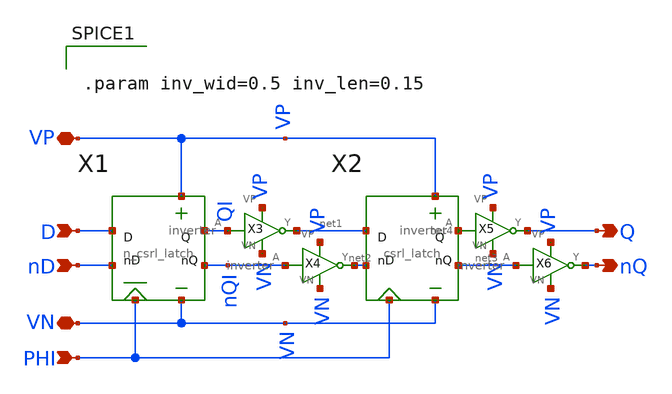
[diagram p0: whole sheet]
** sch_path: dff.sch
**.subckt dff VP D Q nD PHI nQ VN
*.iopin VP
*.ipin D
*.opin Q
*.ipin nD
*.ipin PHI
*.opin nQ
*.iopin VN
X1 VN VP nQI QI PHI nD D n_csrl_latch
X2 VN VP net3 net4 PHI net2 net1 csrl_latch
X3 QI net1 VP VN inverter
X4 nQI net2 VP VN inverter
X5 net4 Q VP VN inverter
X6 net3 nQ VP VN inverter
**** begin user architecture code


.param inv_wid=0.5 inv_len=0.15


**** end user architecture code
**.ends

* expanding   symbol:  n_csrl_latch.sym # of pins=7
** sym_path: n_csrl_latch.sym
** sch_path: n_csrl_latch.sch
.subckt n_csrl_latch VN VP nQ Q PHI nD D
*.ipin D
*.ipin nD
*.opin nQ
*.opin Q
*.ipin PHI
*.iopin VP
*.iopin VN
XM1 VN nD net3 VN sky130_fd_pr__nfet_01v8 L={dff_len} W={dff_wid} nf=1 ad='int((nf+1)/2) * W/nf * 0.29'
+ as='int((nf+2)/2) * W/nf * 0.29' pd='2*int((nf+1)/2) * (W/nf + 0.29)' ps='2*int((nf+2)/2) * (W/nf + 0.29)'
+ nrd='0.29 / W' nrs='0.29 / W' sa=0 sb=0 sd=0 mult=1 m=1
XM2 net3 PHI Q VN sky130_fd_pr__nfet_01v8 L={dff_len} W={dff_wid} nf=1 ad='int((nf+1)/2) * W/nf * 0.29'
+ as='int((nf+2)/2) * W/nf * 0.29' pd='2*int((nf+1)/2) * (W/nf + 0.29)' ps='2*int((nf+2)/2) * (W/nf + 0.29)'
+ nrd='0.29 / W' nrs='0.29 / W' sa=0 sb=0 sd=0 mult=1 m=1
XM3 VN nQ Q VN sky130_fd_pr__nfet_01v8 L={dff_len} W={dff_wid} nf=1 ad='int((nf+1)/2) * W/nf * 0.29'
+ as='int((nf+2)/2) * W/nf * 0.29' pd='2*int((nf+1)/2) * (W/nf + 0.29)' ps='2*int((nf+2)/2) * (W/nf + 0.29)'
+ nrd='0.29 / W' nrs='0.29 / W' sa=0 sb=0 sd=0 mult=1 m=1
XM4 net1 D VN VN sky130_fd_pr__nfet_01v8 L={dff_len} W={dff_wid} nf=1 ad='int((nf+1)/2) * W/nf * 0.29'
+ as='int((nf+2)/2) * W/nf * 0.29' pd='2*int((nf+1)/2) * (W/nf + 0.29)' ps='2*int((nf+2)/2) * (W/nf + 0.29)'
+ nrd='0.29 / W' nrs='0.29 / W' sa=0 sb=0 sd=0 mult=1 m=1
XM5 net1 PHI nQ VN sky130_fd_pr__nfet_01v8 L={dff_len} W={dff_wid} nf=1 ad='int((nf+1)/2) * W/nf * 0.29'
+ as='int((nf+2)/2) * W/nf * 0.29' pd='2*int((nf+1)/2) * (W/nf + 0.29)' ps='2*int((nf+2)/2) * (W/nf + 0.29)'
+ nrd='0.29 / W' nrs='0.29 / W' sa=0 sb=0 sd=0 mult=1 m=1
XM6 VN Q nQ VN sky130_fd_pr__nfet_01v8 L={dff_len} W={dff_wid} nf=1 ad='int((nf+1)/2) * W/nf * 0.29'
+ as='int((nf+2)/2) * W/nf * 0.29' pd='2*int((nf+1)/2) * (W/nf + 0.29)' ps='2*int((nf+2)/2) * (W/nf + 0.29)'
+ nrd='0.29 / W' nrs='0.29 / W' sa=0 sb=0 sd=0 mult=1 m=1
XM13 VP D net2 VP sky130_fd_pr__pfet_01v8 L={dff_len} W={dff_wid} nf=1 ad='int((nf+1)/2) * W/nf * 0.29'
+ as='int((nf+2)/2) * W/nf * 0.29' pd='2*int((nf+1)/2) * (W/nf + 0.29)' ps='2*int((nf+2)/2) * (W/nf + 0.29)'
+ nrd='0.29 / W' nrs='0.29 / W' sa=0 sb=0 sd=0 mult=1 m=1
XM14 net2 PHI VP VP sky130_fd_pr__pfet_01v8 L={dff_len} W={dff_wid} nf=1 ad='int((nf+1)/2) * W/nf * 0.29'
+ as='int((nf+2)/2) * W/nf * 0.29' pd='2*int((nf+1)/2) * (W/nf + 0.29)' ps='2*int((nf+2)/2) * (W/nf + 0.29)'
+ nrd='0.29 / W' nrs='0.29 / W' sa=0 sb=0 sd=0 mult=1 m=1
XM15 nQ Q net2 VP sky130_fd_pr__pfet_01v8 L={dff_len} W={dff_wid} nf=1 ad='int((nf+1)/2) * W/nf * 0.29'
+ as='int((nf+2)/2) * W/nf * 0.29' pd='2*int((nf+1)/2) * (W/nf + 0.29)' ps='2*int((nf+2)/2) * (W/nf + 0.29)'
+ nrd='0.29 / W' nrs='0.29 / W' sa=0 sb=0 sd=0 mult=1 m=1
XM16 net4 nD VP VP sky130_fd_pr__pfet_01v8 L={dff_len} W={dff_wid} nf=1 ad='int((nf+1)/2) * W/nf * 0.29'
+ as='int((nf+2)/2) * W/nf * 0.29' pd='2*int((nf+1)/2) * (W/nf + 0.29)' ps='2*int((nf+2)/2) * (W/nf + 0.29)'
+ nrd='0.29 / W' nrs='0.29 / W' sa=0 sb=0 sd=0 mult=1 m=1
XM17 net4 PHI VP VP sky130_fd_pr__pfet_01v8 L={dff_len} W={dff_wid} nf=1 ad='int((nf+1)/2) * W/nf * 0.29'
+ as='int((nf+2)/2) * W/nf * 0.29' pd='2*int((nf+1)/2) * (W/nf + 0.29)' ps='2*int((nf+2)/2) * (W/nf + 0.29)'
+ nrd='0.29 / W' nrs='0.29 / W' sa=0 sb=0 sd=0 mult=1 m=1
XM18 Q nQ net4 VP sky130_fd_pr__pfet_01v8 L={dff_len} W={dff_wid} nf=1 ad='int((nf+1)/2) * W/nf * 0.29'
+ as='int((nf+2)/2) * W/nf * 0.29' pd='2*int((nf+1)/2) * (W/nf + 0.29)' ps='2*int((nf+2)/2) * (W/nf + 0.29)'
+ nrd='0.29 / W' nrs='0.29 / W' sa=0 sb=0 sd=0 mult=1 m=1
**** begin user architecture code


.param dff_wid=0.5 dff_len=0.5


**** end user architecture code
.ends


* expanding   symbol:  csrl_latch.sym # of pins=7
** sym_path: csrl_latch.sym
** sch_path: csrl_latch.sch
.subckt csrl_latch VN VP nQ Q PHI nD D
*.ipin nD
*.ipin D
*.opin Q
*.opin nQ
*.ipin PHI
*.iopin VP
*.iopin VN
XM7 net3 D VN VN sky130_fd_pr__nfet_01v8 L={dff_len} W={dff_wid} nf=1 ad='int((nf+1)/2) * W/nf * 0.29'
+ as='int((nf+2)/2) * W/nf * 0.29' pd='2*int((nf+1)/2) * (W/nf + 0.29)' ps='2*int((nf+2)/2) * (W/nf + 0.29)'
+ nrd='0.29 / W' nrs='0.29 / W' sa=0 sb=0 sd=0 mult=1 m=1
XM8 VN PHI net3 VN sky130_fd_pr__nfet_01v8 L={dff_len} W={dff_wid} nf=1 ad='int((nf+1)/2) * W/nf * 0.29'
+ as='int((nf+2)/2) * W/nf * 0.29' pd='2*int((nf+1)/2) * (W/nf + 0.29)' ps='2*int((nf+2)/2) * (W/nf + 0.29)'
+ nrd='0.29 / W' nrs='0.29 / W' sa=0 sb=0 sd=0 mult=1 m=1
XM9 nQ Q net3 VN sky130_fd_pr__nfet_01v8 L={dff_len} W={dff_wid} nf=1 ad='int((nf+1)/2) * W/nf * 0.29'
+ as='int((nf+2)/2) * W/nf * 0.29' pd='2*int((nf+1)/2) * (W/nf + 0.29)' ps='2*int((nf+2)/2) * (W/nf + 0.29)'
+ nrd='0.29 / W' nrs='0.29 / W' sa=0 sb=0 sd=0 mult=1 m=1
XM10 VN nD net2 VN sky130_fd_pr__nfet_01v8 L={dff_len} W={dff_wid} nf=1 ad='int((nf+1)/2) * W/nf * 0.29'
+ as='int((nf+2)/2) * W/nf * 0.29' pd='2*int((nf+1)/2) * (W/nf + 0.29)' ps='2*int((nf+2)/2) * (W/nf + 0.29)'
+ nrd='0.29 / W' nrs='0.29 / W' sa=0 sb=0 sd=0 mult=1 m=1
XM11 VN PHI net2 VN sky130_fd_pr__nfet_01v8 L={dff_len} W={dff_wid} nf=1 ad='int((nf+1)/2) * W/nf * 0.29'
+ as='int((nf+2)/2) * W/nf * 0.29' pd='2*int((nf+1)/2) * (W/nf + 0.29)' ps='2*int((nf+2)/2) * (W/nf + 0.29)'
+ nrd='0.29 / W' nrs='0.29 / W' sa=0 sb=0 sd=0 mult=1 m=1
XM12 Q nQ net2 VN sky130_fd_pr__nfet_01v8 L={dff_len} W={dff_wid} nf=1 ad='int((nf+1)/2) * W/nf * 0.29'
+ as='int((nf+2)/2) * W/nf * 0.29' pd='2*int((nf+1)/2) * (W/nf + 0.29)' ps='2*int((nf+2)/2) * (W/nf + 0.29)'
+ nrd='0.29 / W' nrs='0.29 / W' sa=0 sb=0 sd=0 mult=1 m=1
XM19 net1 nD VP VP sky130_fd_pr__pfet_01v8 L={dff_len} W={dff_wid} nf=1 ad='int((nf+1)/2) * W/nf * 0.29'
+ as='int((nf+2)/2) * W/nf * 0.29' pd='2*int((nf+1)/2) * (W/nf + 0.29)' ps='2*int((nf+2)/2) * (W/nf + 0.29)'
+ nrd='0.29 / W' nrs='0.29 / W' sa=0 sb=0 sd=0 mult=1 m=1
XM20 Q PHI net1 VP sky130_fd_pr__pfet_01v8 L={dff_len} W={dff_wid} nf=1 ad='int((nf+1)/2) * W/nf * 0.29'
+ as='int((nf+2)/2) * W/nf * 0.29' pd='2*int((nf+1)/2) * (W/nf + 0.29)' ps='2*int((nf+2)/2) * (W/nf + 0.29)'
+ nrd='0.29 / W' nrs='0.29 / W' sa=0 sb=0 sd=0 mult=1 m=1
XM21 VP nQ Q VP sky130_fd_pr__pfet_01v8 L={dff_len} W={dff_wid} nf=1 ad='int((nf+1)/2) * W/nf * 0.29'
+ as='int((nf+2)/2) * W/nf * 0.29' pd='2*int((nf+1)/2) * (W/nf + 0.29)' ps='2*int((nf+2)/2) * (W/nf + 0.29)'
+ nrd='0.29 / W' nrs='0.29 / W' sa=0 sb=0 sd=0 mult=1 m=1
XM22 VP D net4 VP sky130_fd_pr__pfet_01v8 L={dff_len} W={dff_wid} nf=1 ad='int((nf+1)/2) * W/nf * 0.29'
+ as='int((nf+2)/2) * W/nf * 0.29' pd='2*int((nf+1)/2) * (W/nf + 0.29)' ps='2*int((nf+2)/2) * (W/nf + 0.29)'
+ nrd='0.29 / W' nrs='0.29 / W' sa=0 sb=0 sd=0 mult=1 m=1
XM23 nQ PHI net4 VP sky130_fd_pr__pfet_01v8 L={dff_len} W={dff_wid} nf=1 ad='int((nf+1)/2) * W/nf * 0.29'
+ as='int((nf+2)/2) * W/nf * 0.29' pd='2*int((nf+1)/2) * (W/nf + 0.29)' ps='2*int((nf+2)/2) * (W/nf + 0.29)'
+ nrd='0.29 / W' nrs='0.29 / W' sa=0 sb=0 sd=0 mult=1 m=1
XM24 VP Q nQ VP sky130_fd_pr__pfet_01v8 L={dff_len} W={dff_wid} nf=1 ad='int((nf+1)/2) * W/nf * 0.29'
+ as='int((nf+2)/2) * W/nf * 0.29' pd='2*int((nf+1)/2) * (W/nf + 0.29)' ps='2*int((nf+2)/2) * (W/nf + 0.29)'
+ nrd='0.29 / W' nrs='0.29 / W' sa=0 sb=0 sd=0 mult=1 m=1
.ends


* expanding   symbol:  inverter.sym # of pins=4
** sym_path: inverter.sym
** sch_path: inverter.sch
.subckt inverter A Y VP VN
*.iopin VP
*.ipin A
*.opin Y
*.iopin VN
XM2 Y A VP VP sky130_fd_pr__pfet_01v8 L={inv_len} W={inv_wid} nf=1 ad='int((nf+1)/2) * W/nf * 0.29' as='int((nf+2)/2) * W/nf * 0.29'
+ pd='2*int((nf+1)/2) * (W/nf + 0.29)' ps='2*int((nf+2)/2) * (W/nf + 0.29)' nrd='0.29 / W' nrs='0.29 / W'
+ sa=0 sb=0 sd=0 mult=1 m=1
XM1 Y A VN VN sky130_fd_pr__nfet_01v8 L={inv_len} W={inv_wid} nf=1 ad='int((nf+1)/2) * W/nf * 0.29' as='int((nf+2)/2) * W/nf * 0.29'
+ pd='2*int((nf+1)/2) * (W/nf + 0.29)' ps='2*int((nf+2)/2) * (W/nf + 0.29)' nrd='0.29 / W' nrs='0.29 / W'
+ sa=0 sb=0 sd=0 mult=1 m=1
.ends

.end
